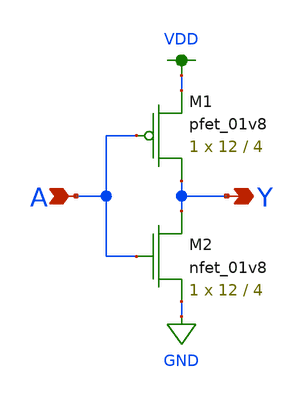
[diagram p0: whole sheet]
** sch_path: xschem/inverter.sch
**.subckt inverter A Y
*.ipin A
*.opin Y
XM1 Y A VDD VDD sky130_fd_pr__pfet_01v8 L=4 W=12 nf=1 ad='int((nf+1)/2) * W/nf * 0.29' as='int((nf+2)/2) * W/nf * 0.29'
+ pd='2*int((nf+1)/2) * (W/nf + 0.29)' ps='2*int((nf+2)/2) * (W/nf + 0.29)' nrd='0.29 / W' nrs='0.29 / W'
+ sa=0 sb=0 sd=0 mult=1 m=1
XM2 Y A GND GND sky130_fd_pr__nfet_01v8 L=4 W=12 nf=1 ad='int((nf+1)/2) * W/nf * 0.29' as='int((nf+2)/2) * W/nf * 0.29'
+ pd='2*int((nf+1)/2) * (W/nf + 0.29)' ps='2*int((nf+2)/2) * (W/nf + 0.29)' nrd='0.29 / W' nrs='0.29 / W'
+ sa=0 sb=0 sd=0 mult=1 m=1
**.ends
.GLOBAL GND
.GLOBAL VDD
.end
